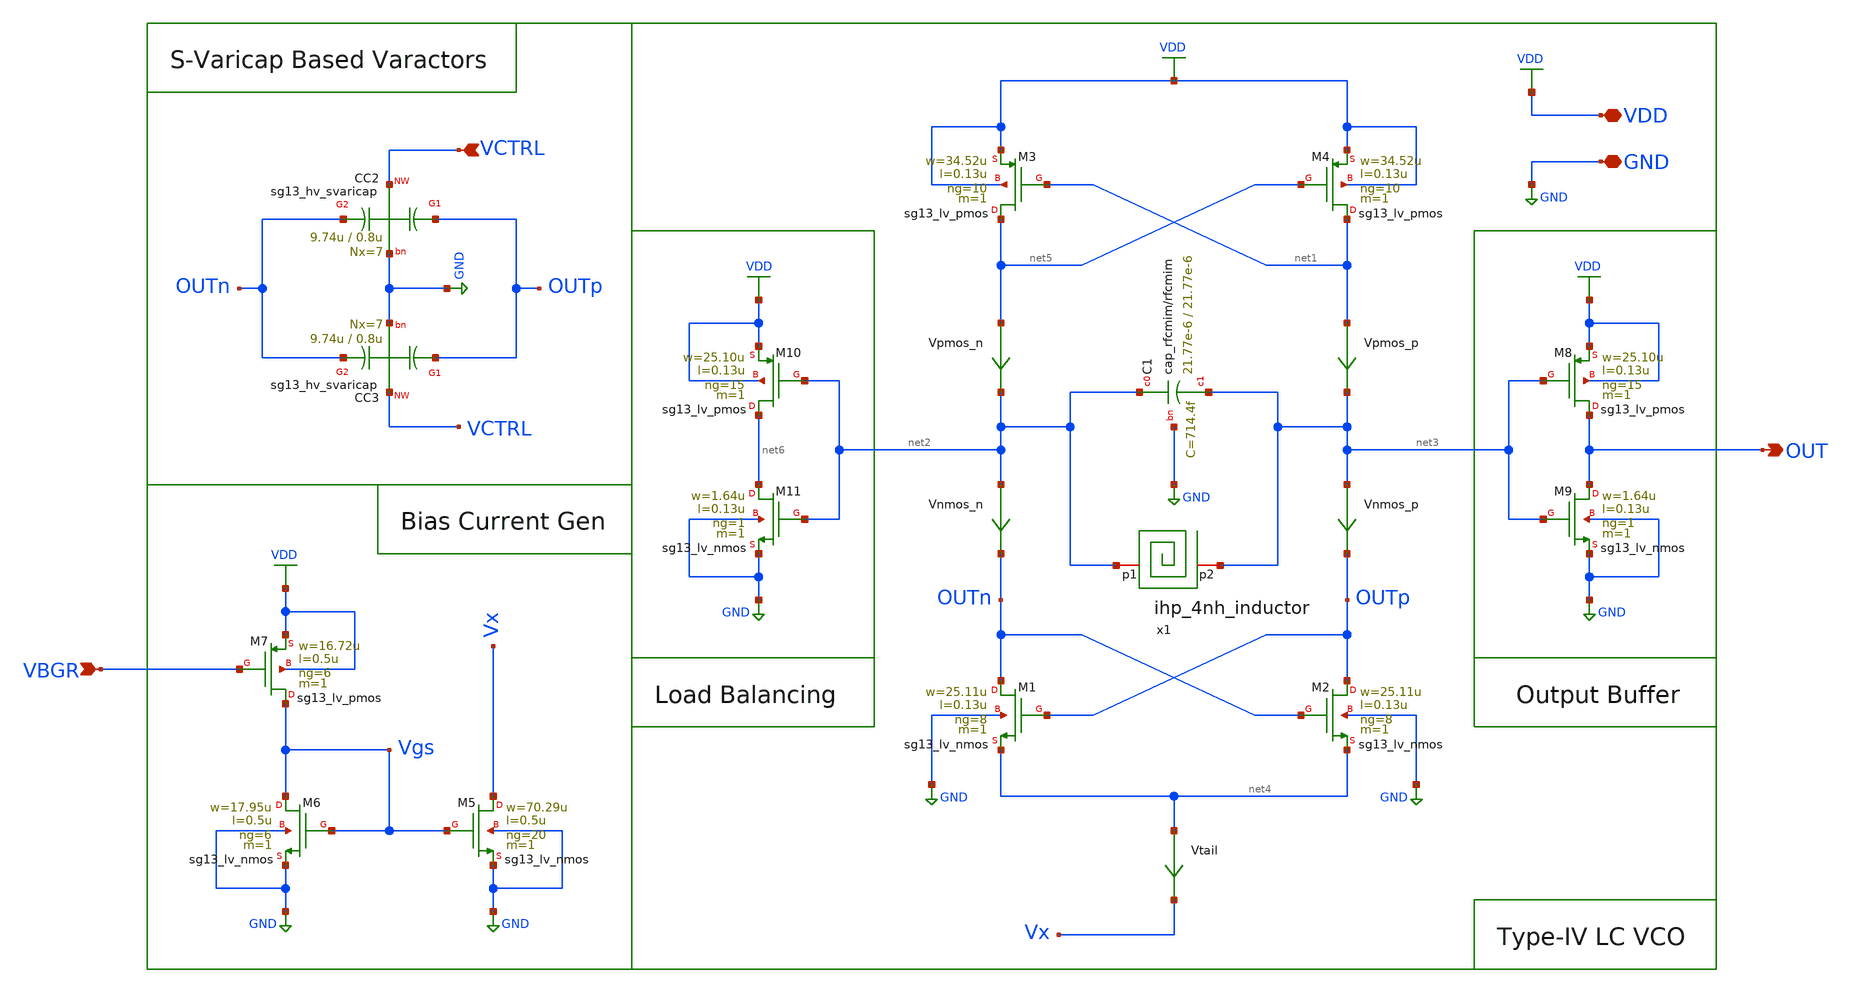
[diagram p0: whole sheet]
** sch_path: schematic/lc-vco/LC_VCO_standalone.sch
**.subckt LC_VCO_standalone OUT VCTRL VBGR VDD GND
*.opin OUT
*.ipin VCTRL
*.ipin VBGR
*.iopin VDD
*.iopin GND
XM5 Vx Vgs GND GND sg13_lv_nmos w=70.29u l=0.5u ng=20 m=1 mm_ok=1
XM4 net1 net5 VDD VDD sg13_lv_pmos w=34.52u l=0.13u ng=10 m=1 mm_ok=1
XM3 net5 net1 VDD VDD sg13_lv_pmos w=34.52u l=0.13u ng=10 m=1 mm_ok=1
XM2 OUTp OUTn net4 GND sg13_lv_nmos w=25.11u l=0.13u ng=8 m=1 mm_ok=1
XM1 OUTn OUTp net4 GND sg13_lv_nmos w=25.11u l=0.13u ng=8 m=1 mm_ok=1
Vpmos_p net1 net3 0
.save i(vpmos_p)
Vnmos_p net3 OUTp 0
.save i(vnmos_p)
Vtail net4 Vx 0
.save i(vtail)
XM6 Vgs Vgs GND GND sg13_lv_nmos w=17.95u l=0.5u ng=6 m=1 mm_ok=1
Vpmos_n net5 net2 0
.save i(vpmos_n)
Vnmos_n net2 OUTn 0
.save i(vnmos_n)
x1 net2 net3 ihp_4nh_inductor
XC1 net2 net3 GND cap_rfcmim w=21.77e-6 l=21.77e-6 wfeed=10.0e-6 m=1 mm_ok=1
XC3 OUTp VCTRL OUTn GND sg13_hv_svaricap w=9.74u l=0.8u Nx=7
XC2 OUTp VCTRL OUTn GND sg13_hv_svaricap w=9.74u l=0.8u Nx=7
XM7 Vgs VBGR VDD VDD sg13_lv_pmos w=16.72u l=0.5u ng=6 m=1 mm_ok=1
XM8 OUT net3 VDD VDD sg13_lv_pmos w=25.10u l=0.13u ng=15 m=1 mm_ok=1
XM9 OUT net3 GND GND sg13_lv_nmos w=1.64u l=0.13u ng=1 m=1 mm_ok=1
XM10 net6 net2 VDD VDD sg13_lv_pmos w=25.10u l=0.13u ng=15 m=1 mm_ok=1
XM11 net6 net2 GND GND sg13_lv_nmos w=1.64u l=0.13u ng=1 m=1 mm_ok=1
**.ends
.GLOBAL VDD
.GLOBAL GND
.end
